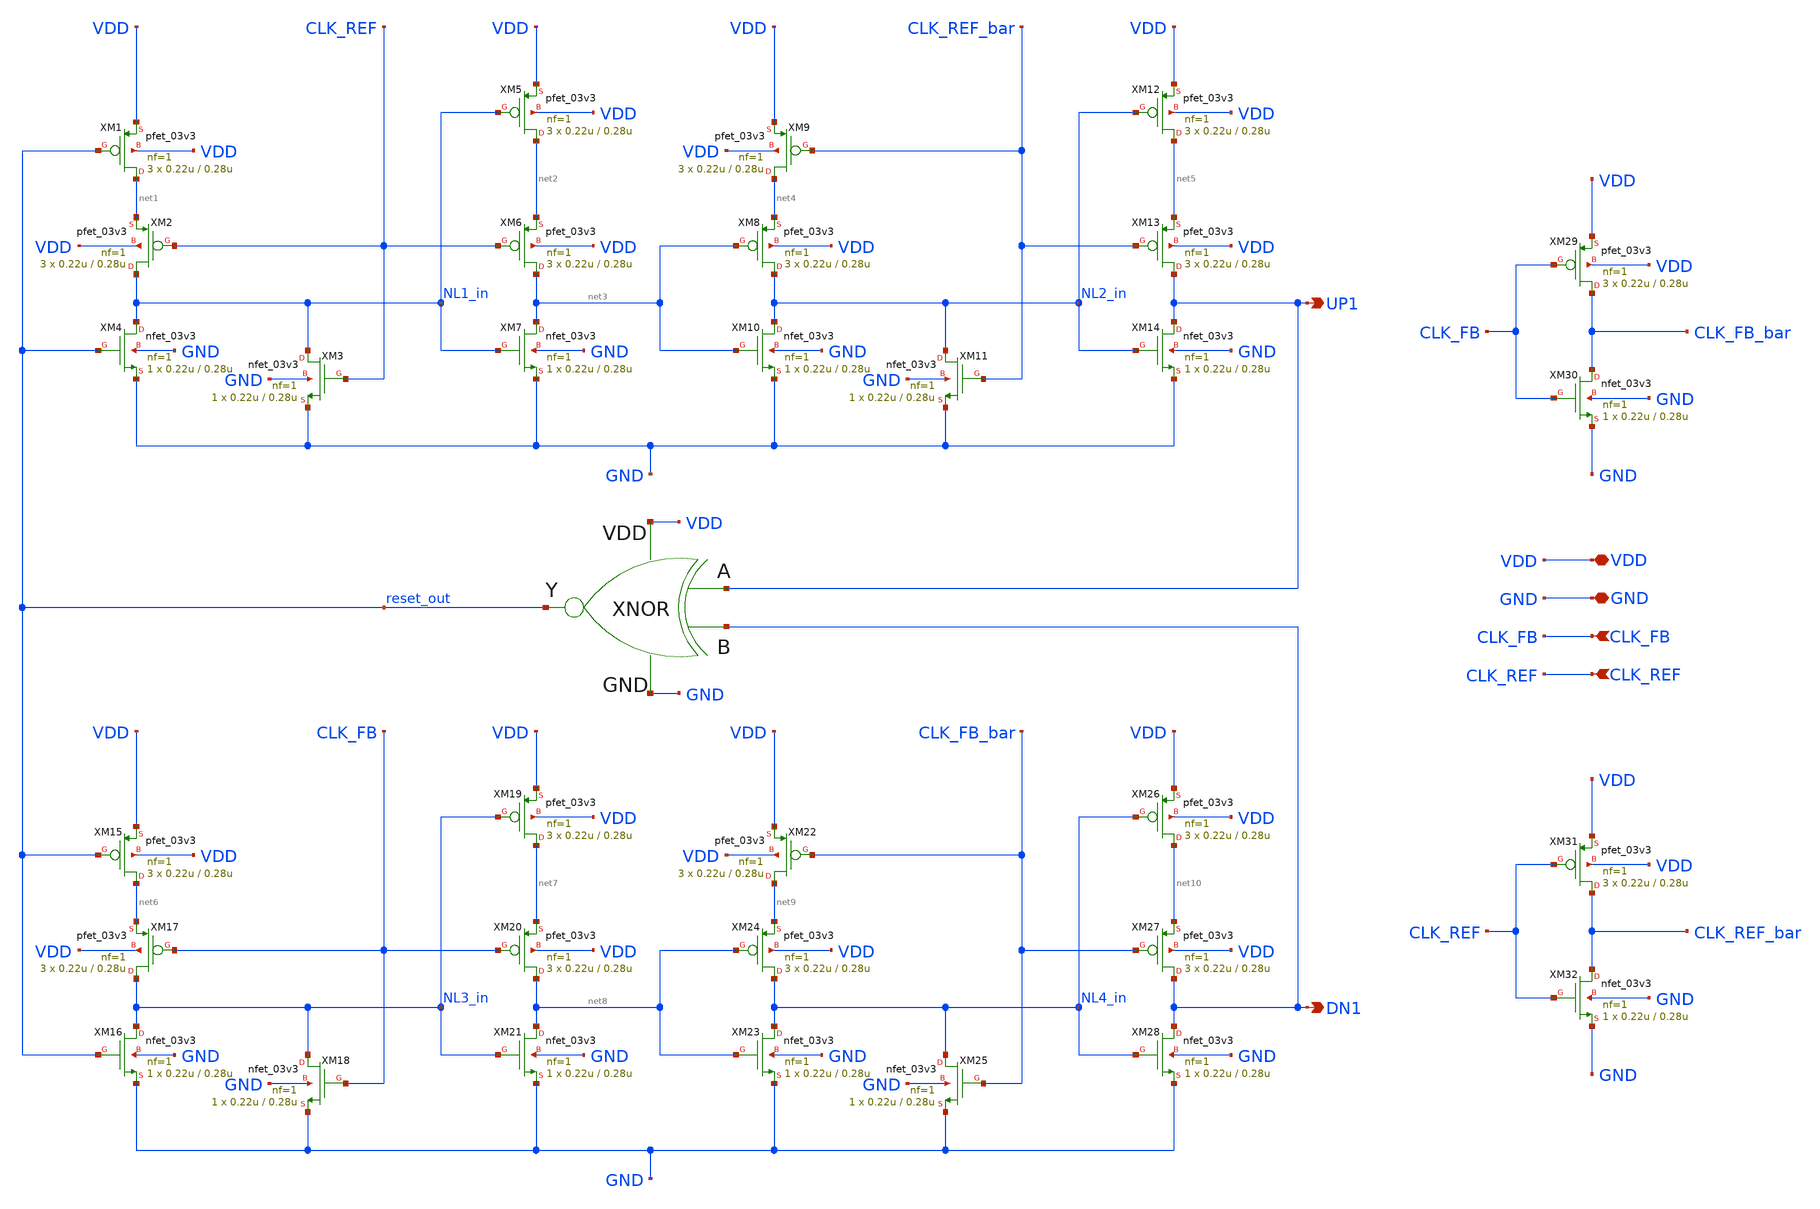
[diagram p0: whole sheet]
** sch_path: PFD/FTL_PFD.sch
**.subckt FTL_PFD UP1 DN1 CLK_FB CLK_REF VDD GND
*.opin UP1
*.opin DN1
*.ipin CLK_FB
*.ipin CLK_REF
*.iopin VDD
*.iopin GND
XM1 net1 reset_out VDD VDD pfet_03v3 L=0.28u W=0.22u nf=1 ad='int((nf+1)/2) * W/nf * 0.18u' as='int((nf+2)/2) * W/nf * 0.18u'
+ pd='2*int((nf+1)/2) * (W/nf + 0.18u)' ps='2*int((nf+2)/2) * (W/nf + 0.18u)' nrd='0.18u / W' nrs='0.18u / W'
+ sa=0 sb=0 sd=0 m=3
XM4 NL1_in reset_out GND GND nfet_03v3 L=0.28u W=0.22u nf=1 ad='int((nf+1)/2) * W/nf * 0.18u' as='int((nf+2)/2) * W/nf * 0.18u'
+ pd='2*int((nf+1)/2) * (W/nf + 0.18u)' ps='2*int((nf+2)/2) * (W/nf + 0.18u)' nrd='0.18u / W' nrs='0.18u / W'
+ sa=0 sb=0 sd=0 m=1
XM2 NL1_in CLK_REF net1 VDD pfet_03v3 L=0.28u W=0.22u nf=1 ad='int((nf+1)/2) * W/nf * 0.18u' as='int((nf+2)/2) * W/nf * 0.18u'
+ pd='2*int((nf+1)/2) * (W/nf + 0.18u)' ps='2*int((nf+2)/2) * (W/nf + 0.18u)' nrd='0.18u / W' nrs='0.18u / W'
+ sa=0 sb=0 sd=0 m=3
XM3 NL1_in CLK_REF GND GND nfet_03v3 L=0.28u W=0.22u nf=1 ad='int((nf+1)/2) * W/nf * 0.18u' as='int((nf+2)/2) * W/nf * 0.18u'
+ pd='2*int((nf+1)/2) * (W/nf + 0.18u)' ps='2*int((nf+2)/2) * (W/nf + 0.18u)' nrd='0.18u / W' nrs='0.18u / W'
+ sa=0 sb=0 sd=0 m=1
XM5 net2 NL1_in VDD VDD pfet_03v3 L=0.28u W=0.22u nf=1 ad='int((nf+1)/2) * W/nf * 0.18u' as='int((nf+2)/2) * W/nf * 0.18u'
+ pd='2*int((nf+1)/2) * (W/nf + 0.18u)' ps='2*int((nf+2)/2) * (W/nf + 0.18u)' nrd='0.18u / W' nrs='0.18u / W'
+ sa=0 sb=0 sd=0 m=3
XM6 net3 CLK_REF net2 VDD pfet_03v3 L=0.28u W=0.22u nf=1 ad='int((nf+1)/2) * W/nf * 0.18u' as='int((nf+2)/2) * W/nf * 0.18u'
+ pd='2*int((nf+1)/2) * (W/nf + 0.18u)' ps='2*int((nf+2)/2) * (W/nf + 0.18u)' nrd='0.18u / W' nrs='0.18u / W'
+ sa=0 sb=0 sd=0 m=3
XM7 net3 NL1_in GND GND nfet_03v3 L=0.28u W=0.22u nf=1 ad='int((nf+1)/2) * W/nf * 0.18u' as='int((nf+2)/2) * W/nf * 0.18u'
+ pd='2*int((nf+1)/2) * (W/nf + 0.18u)' ps='2*int((nf+2)/2) * (W/nf + 0.18u)' nrd='0.18u / W' nrs='0.18u / W'
+ sa=0 sb=0 sd=0 m=1
XM9 net4 CLK_REF_bar VDD VDD pfet_03v3 L=0.28u W=0.22u nf=1 ad='int((nf+1)/2) * W/nf * 0.18u' as='int((nf+2)/2) * W/nf * 0.18u'
+ pd='2*int((nf+1)/2) * (W/nf + 0.18u)' ps='2*int((nf+2)/2) * (W/nf + 0.18u)' nrd='0.18u / W' nrs='0.18u / W'
+ sa=0 sb=0 sd=0 m=3
XM10 NL2_in net3 GND GND nfet_03v3 L=0.28u W=0.22u nf=1 ad='int((nf+1)/2) * W/nf * 0.18u' as='int((nf+2)/2) * W/nf * 0.18u'
+ pd='2*int((nf+1)/2) * (W/nf + 0.18u)' ps='2*int((nf+2)/2) * (W/nf + 0.18u)' nrd='0.18u / W' nrs='0.18u / W'
+ sa=0 sb=0 sd=0 m=1
XM8 NL2_in net3 net4 VDD pfet_03v3 L=0.28u W=0.22u nf=1 ad='int((nf+1)/2) * W/nf * 0.18u' as='int((nf+2)/2) * W/nf * 0.18u'
+ pd='2*int((nf+1)/2) * (W/nf + 0.18u)' ps='2*int((nf+2)/2) * (W/nf + 0.18u)' nrd='0.18u / W' nrs='0.18u / W'
+ sa=0 sb=0 sd=0 m=3
XM11 NL2_in CLK_REF_bar GND GND nfet_03v3 L=0.28u W=0.22u nf=1 ad='int((nf+1)/2) * W/nf * 0.18u' as='int((nf+2)/2) * W/nf * 0.18u'
+ pd='2*int((nf+1)/2) * (W/nf + 0.18u)' ps='2*int((nf+2)/2) * (W/nf + 0.18u)' nrd='0.18u / W' nrs='0.18u / W'
+ sa=0 sb=0 sd=0 m=1
XM12 net5 NL2_in VDD VDD pfet_03v3 L=0.28u W=0.22u nf=1 ad='int((nf+1)/2) * W/nf * 0.18u' as='int((nf+2)/2) * W/nf * 0.18u'
+ pd='2*int((nf+1)/2) * (W/nf + 0.18u)' ps='2*int((nf+2)/2) * (W/nf + 0.18u)' nrd='0.18u / W' nrs='0.18u / W'
+ sa=0 sb=0 sd=0 m=3
XM13 UP1 CLK_REF_bar net5 VDD pfet_03v3 L=0.28u W=0.22u nf=1 ad='int((nf+1)/2) * W/nf * 0.18u' as='int((nf+2)/2) * W/nf * 0.18u'
+ pd='2*int((nf+1)/2) * (W/nf + 0.18u)' ps='2*int((nf+2)/2) * (W/nf + 0.18u)' nrd='0.18u / W' nrs='0.18u / W'
+ sa=0 sb=0 sd=0 m=3
XM14 UP1 NL2_in GND GND nfet_03v3 L=0.28u W=0.22u nf=1 ad='int((nf+1)/2) * W/nf * 0.18u' as='int((nf+2)/2) * W/nf * 0.18u'
+ pd='2*int((nf+1)/2) * (W/nf + 0.18u)' ps='2*int((nf+2)/2) * (W/nf + 0.18u)' nrd='0.18u / W' nrs='0.18u / W'
+ sa=0 sb=0 sd=0 m=1
XM15 net6 reset_out VDD VDD pfet_03v3 L=0.28u W=0.22u nf=1 ad='int((nf+1)/2) * W/nf * 0.18u' as='int((nf+2)/2) * W/nf * 0.18u'
+ pd='2*int((nf+1)/2) * (W/nf + 0.18u)' ps='2*int((nf+2)/2) * (W/nf + 0.18u)' nrd='0.18u / W' nrs='0.18u / W'
+ sa=0 sb=0 sd=0 m=3
XM16 NL3_in reset_out GND GND nfet_03v3 L=0.28u W=0.22u nf=1 ad='int((nf+1)/2) * W/nf * 0.18u' as='int((nf+2)/2) * W/nf * 0.18u'
+ pd='2*int((nf+1)/2) * (W/nf + 0.18u)' ps='2*int((nf+2)/2) * (W/nf + 0.18u)' nrd='0.18u / W' nrs='0.18u / W'
+ sa=0 sb=0 sd=0 m=1
XM17 NL3_in CLK_FB net6 VDD pfet_03v3 L=0.28u W=0.22u nf=1 ad='int((nf+1)/2) * W/nf * 0.18u' as='int((nf+2)/2) * W/nf * 0.18u'
+ pd='2*int((nf+1)/2) * (W/nf + 0.18u)' ps='2*int((nf+2)/2) * (W/nf + 0.18u)' nrd='0.18u / W' nrs='0.18u / W'
+ sa=0 sb=0 sd=0 m=3
XM18 NL3_in CLK_FB GND GND nfet_03v3 L=0.28u W=0.22u nf=1 ad='int((nf+1)/2) * W/nf * 0.18u' as='int((nf+2)/2) * W/nf * 0.18u'
+ pd='2*int((nf+1)/2) * (W/nf + 0.18u)' ps='2*int((nf+2)/2) * (W/nf + 0.18u)' nrd='0.18u / W' nrs='0.18u / W'
+ sa=0 sb=0 sd=0 m=1
XM19 net7 NL3_in VDD VDD pfet_03v3 L=0.28u W=0.22u nf=1 ad='int((nf+1)/2) * W/nf * 0.18u' as='int((nf+2)/2) * W/nf * 0.18u'
+ pd='2*int((nf+1)/2) * (W/nf + 0.18u)' ps='2*int((nf+2)/2) * (W/nf + 0.18u)' nrd='0.18u / W' nrs='0.18u / W'
+ sa=0 sb=0 sd=0 m=3
XM20 net8 CLK_FB net7 VDD pfet_03v3 L=0.28u W=0.22u nf=1 ad='int((nf+1)/2) * W/nf * 0.18u' as='int((nf+2)/2) * W/nf * 0.18u'
+ pd='2*int((nf+1)/2) * (W/nf + 0.18u)' ps='2*int((nf+2)/2) * (W/nf + 0.18u)' nrd='0.18u / W' nrs='0.18u / W'
+ sa=0 sb=0 sd=0 m=3
XM21 net8 NL3_in GND GND nfet_03v3 L=0.28u W=0.22u nf=1 ad='int((nf+1)/2) * W/nf * 0.18u' as='int((nf+2)/2) * W/nf * 0.18u'
+ pd='2*int((nf+1)/2) * (W/nf + 0.18u)' ps='2*int((nf+2)/2) * (W/nf + 0.18u)' nrd='0.18u / W' nrs='0.18u / W'
+ sa=0 sb=0 sd=0 m=1
XM22 net9 CLK_FB_bar VDD VDD pfet_03v3 L=0.28u W=0.22u nf=1 ad='int((nf+1)/2) * W/nf * 0.18u' as='int((nf+2)/2) * W/nf * 0.18u'
+ pd='2*int((nf+1)/2) * (W/nf + 0.18u)' ps='2*int((nf+2)/2) * (W/nf + 0.18u)' nrd='0.18u / W' nrs='0.18u / W'
+ sa=0 sb=0 sd=0 m=3
XM23 NL4_in net8 GND GND nfet_03v3 L=0.28u W=0.22u nf=1 ad='int((nf+1)/2) * W/nf * 0.18u' as='int((nf+2)/2) * W/nf * 0.18u'
+ pd='2*int((nf+1)/2) * (W/nf + 0.18u)' ps='2*int((nf+2)/2) * (W/nf + 0.18u)' nrd='0.18u / W' nrs='0.18u / W'
+ sa=0 sb=0 sd=0 m=1
XM24 NL4_in net8 net9 VDD pfet_03v3 L=0.28u W=0.22u nf=1 ad='int((nf+1)/2) * W/nf * 0.18u' as='int((nf+2)/2) * W/nf * 0.18u'
+ pd='2*int((nf+1)/2) * (W/nf + 0.18u)' ps='2*int((nf+2)/2) * (W/nf + 0.18u)' nrd='0.18u / W' nrs='0.18u / W'
+ sa=0 sb=0 sd=0 m=3
XM25 NL4_in CLK_FB_bar GND GND nfet_03v3 L=0.28u W=0.22u nf=1 ad='int((nf+1)/2) * W/nf * 0.18u' as='int((nf+2)/2) * W/nf * 0.18u'
+ pd='2*int((nf+1)/2) * (W/nf + 0.18u)' ps='2*int((nf+2)/2) * (W/nf + 0.18u)' nrd='0.18u / W' nrs='0.18u / W'
+ sa=0 sb=0 sd=0 m=1
XM26 net10 NL4_in VDD VDD pfet_03v3 L=0.28u W=0.22u nf=1 ad='int((nf+1)/2) * W/nf * 0.18u' as='int((nf+2)/2) * W/nf * 0.18u'
+ pd='2*int((nf+1)/2) * (W/nf + 0.18u)' ps='2*int((nf+2)/2) * (W/nf + 0.18u)' nrd='0.18u / W' nrs='0.18u / W'
+ sa=0 sb=0 sd=0 m=3
XM27 DN1 CLK_FB_bar net10 VDD pfet_03v3 L=0.28u W=0.22u nf=1 ad='int((nf+1)/2) * W/nf * 0.18u' as='int((nf+2)/2) * W/nf * 0.18u'
+ pd='2*int((nf+1)/2) * (W/nf + 0.18u)' ps='2*int((nf+2)/2) * (W/nf + 0.18u)' nrd='0.18u / W' nrs='0.18u / W'
+ sa=0 sb=0 sd=0 m=3
XM28 DN1 NL4_in GND GND nfet_03v3 L=0.28u W=0.22u nf=1 ad='int((nf+1)/2) * W/nf * 0.18u' as='int((nf+2)/2) * W/nf * 0.18u'
+ pd='2*int((nf+1)/2) * (W/nf + 0.18u)' ps='2*int((nf+2)/2) * (W/nf + 0.18u)' nrd='0.18u / W' nrs='0.18u / W'
+ sa=0 sb=0 sd=0 m=1
x1 GND UP1 DN1 VDD reset_out XNOR
XM29 CLK_FB_bar CLK_FB VDD VDD pfet_03v3 L=0.28u W=0.22u nf=1 ad='int((nf+1)/2) * W/nf * 0.18u' as='int((nf+2)/2) * W/nf * 0.18u'
+ pd='2*int((nf+1)/2) * (W/nf + 0.18u)' ps='2*int((nf+2)/2) * (W/nf + 0.18u)' nrd='0.18u / W' nrs='0.18u / W'
+ sa=0 sb=0 sd=0 m=3
XM30 CLK_FB_bar CLK_FB GND GND nfet_03v3 L=0.28u W=0.22u nf=1 ad='int((nf+1)/2) * W/nf * 0.18u' as='int((nf+2)/2) * W/nf * 0.18u'
+ pd='2*int((nf+1)/2) * (W/nf + 0.18u)' ps='2*int((nf+2)/2) * (W/nf + 0.18u)' nrd='0.18u / W' nrs='0.18u / W'
+ sa=0 sb=0 sd=0 m=1
XM31 CLK_REF_bar CLK_REF VDD VDD pfet_03v3 L=0.28u W=0.22u nf=1 ad='int((nf+1)/2) * W/nf * 0.18u' as='int((nf+2)/2) * W/nf * 0.18u'
+ pd='2*int((nf+1)/2) * (W/nf + 0.18u)' ps='2*int((nf+2)/2) * (W/nf + 0.18u)' nrd='0.18u / W' nrs='0.18u / W'
+ sa=0 sb=0 sd=0 m=3
XM32 CLK_REF_bar CLK_REF GND GND nfet_03v3 L=0.28u W=0.22u nf=1 ad='int((nf+1)/2) * W/nf * 0.18u' as='int((nf+2)/2) * W/nf * 0.18u'
+ pd='2*int((nf+1)/2) * (W/nf + 0.18u)' ps='2*int((nf+2)/2) * (W/nf + 0.18u)' nrd='0.18u / W' nrs='0.18u / W'
+ sa=0 sb=0 sd=0 m=1
**.ends

* expanding   symbol:  XNOR.sym # of pins=5
** sym_path: PFD/XNOR.sym
** sch_path: PFD/XNOR.sch
.subckt XNOR GND A B VDD Y
*.opin Y
*.ipin A
*.ipin B
*.iopin VDD
*.iopin GND
XM1 net1 A VDD VDD pfet_03v3 L=0.28u W=0.22u nf=1 ad='int((nf+1)/2) * W/nf * 0.18u' as='int((nf+2)/2) * W/nf * 0.18u'
+ pd='2*int((nf+1)/2) * (W/nf + 0.18u)' ps='2*int((nf+2)/2) * (W/nf + 0.18u)' nrd='0.18u / W' nrs='0.18u / W'
+ sa=0 sb=0 sd=0 m=1
XM2 Y A_bar net1 VDD pfet_03v3 L=0.28u W=0.22u nf=1 ad='int((nf+1)/2) * W/nf * 0.18u' as='int((nf+2)/2) * W/nf * 0.18u'
+ pd='2*int((nf+1)/2) * (W/nf + 0.18u)' ps='2*int((nf+2)/2) * (W/nf + 0.18u)' nrd='0.18u / W' nrs='0.18u / W'
+ sa=0 sb=0 sd=0 m=1
XM3 Y B_bar net2 GND nfet_03v3 L=0.28u W=0.22u nf=1 ad='int((nf+1)/2) * W/nf * 0.18u' as='int((nf+2)/2) * W/nf * 0.18u'
+ pd='2*int((nf+1)/2) * (W/nf + 0.18u)' ps='2*int((nf+2)/2) * (W/nf + 0.18u)' nrd='0.18u / W' nrs='0.18u / W'
+ sa=0 sb=0 sd=0 m=1
XM4 net2 A GND GND nfet_03v3 L=0.28u W=0.22u nf=1 ad='int((nf+1)/2) * W/nf * 0.18u' as='int((nf+2)/2) * W/nf * 0.18u'
+ pd='2*int((nf+1)/2) * (W/nf + 0.18u)' ps='2*int((nf+2)/2) * (W/nf + 0.18u)' nrd='0.18u / W' nrs='0.18u / W'
+ sa=0 sb=0 sd=0 m=1
XM5 net3 B_bar VDD VDD pfet_03v3 L=0.28u W=0.22u nf=1 ad='int((nf+1)/2) * W/nf * 0.18u' as='int((nf+2)/2) * W/nf * 0.18u'
+ pd='2*int((nf+1)/2) * (W/nf + 0.18u)' ps='2*int((nf+2)/2) * (W/nf + 0.18u)' nrd='0.18u / W' nrs='0.18u / W'
+ sa=0 sb=0 sd=0 m=1
XM6 Y B net3 VDD pfet_03v3 L=0.28u W=0.22u nf=1 ad='int((nf+1)/2) * W/nf * 0.18u' as='int((nf+2)/2) * W/nf * 0.18u'
+ pd='2*int((nf+1)/2) * (W/nf + 0.18u)' ps='2*int((nf+2)/2) * (W/nf + 0.18u)' nrd='0.18u / W' nrs='0.18u / W'
+ sa=0 sb=0 sd=0 m=1
XM7 Y A_bar net4 GND nfet_03v3 L=0.28u W=0.22u nf=1 ad='int((nf+1)/2) * W/nf * 0.18u' as='int((nf+2)/2) * W/nf * 0.18u'
+ pd='2*int((nf+1)/2) * (W/nf + 0.18u)' ps='2*int((nf+2)/2) * (W/nf + 0.18u)' nrd='0.18u / W' nrs='0.18u / W'
+ sa=0 sb=0 sd=0 m=1
XM8 net4 B GND GND nfet_03v3 L=0.28u W=0.22u nf=1 ad='int((nf+1)/2) * W/nf * 0.18u' as='int((nf+2)/2) * W/nf * 0.18u'
+ pd='2*int((nf+1)/2) * (W/nf + 0.18u)' ps='2*int((nf+2)/2) * (W/nf + 0.18u)' nrd='0.18u / W' nrs='0.18u / W'
+ sa=0 sb=0 sd=0 m=1
XM9 A_bar A VDD VDD pfet_03v3 L=0.28u W=0.22u nf=1 ad='int((nf+1)/2) * W/nf * 0.18u' as='int((nf+2)/2) * W/nf * 0.18u'
+ pd='2*int((nf+1)/2) * (W/nf + 0.18u)' ps='2*int((nf+2)/2) * (W/nf + 0.18u)' nrd='0.18u / W' nrs='0.18u / W'
+ sa=0 sb=0 sd=0 m=3
XM10 A_bar A GND GND nfet_03v3 L=0.28u W=0.22u nf=1 ad='int((nf+1)/2) * W/nf * 0.18u' as='int((nf+2)/2) * W/nf * 0.18u'
+ pd='2*int((nf+1)/2) * (W/nf + 0.18u)' ps='2*int((nf+2)/2) * (W/nf + 0.18u)' nrd='0.18u / W' nrs='0.18u / W'
+ sa=0 sb=0 sd=0 m=1
XM11 B_bar B VDD VDD pfet_03v3 L=0.28u W=0.22u nf=1 ad='int((nf+1)/2) * W/nf * 0.18u' as='int((nf+2)/2) * W/nf * 0.18u'
+ pd='2*int((nf+1)/2) * (W/nf + 0.18u)' ps='2*int((nf+2)/2) * (W/nf + 0.18u)' nrd='0.18u / W' nrs='0.18u / W'
+ sa=0 sb=0 sd=0 m=3
XM12 B_bar B GND GND nfet_03v3 L=0.28u W=0.22u nf=1 ad='int((nf+1)/2) * W/nf * 0.18u' as='int((nf+2)/2) * W/nf * 0.18u'
+ pd='2*int((nf+1)/2) * (W/nf + 0.18u)' ps='2*int((nf+2)/2) * (W/nf + 0.18u)' nrd='0.18u / W' nrs='0.18u / W'
+ sa=0 sb=0 sd=0 m=1
.ends

.end
